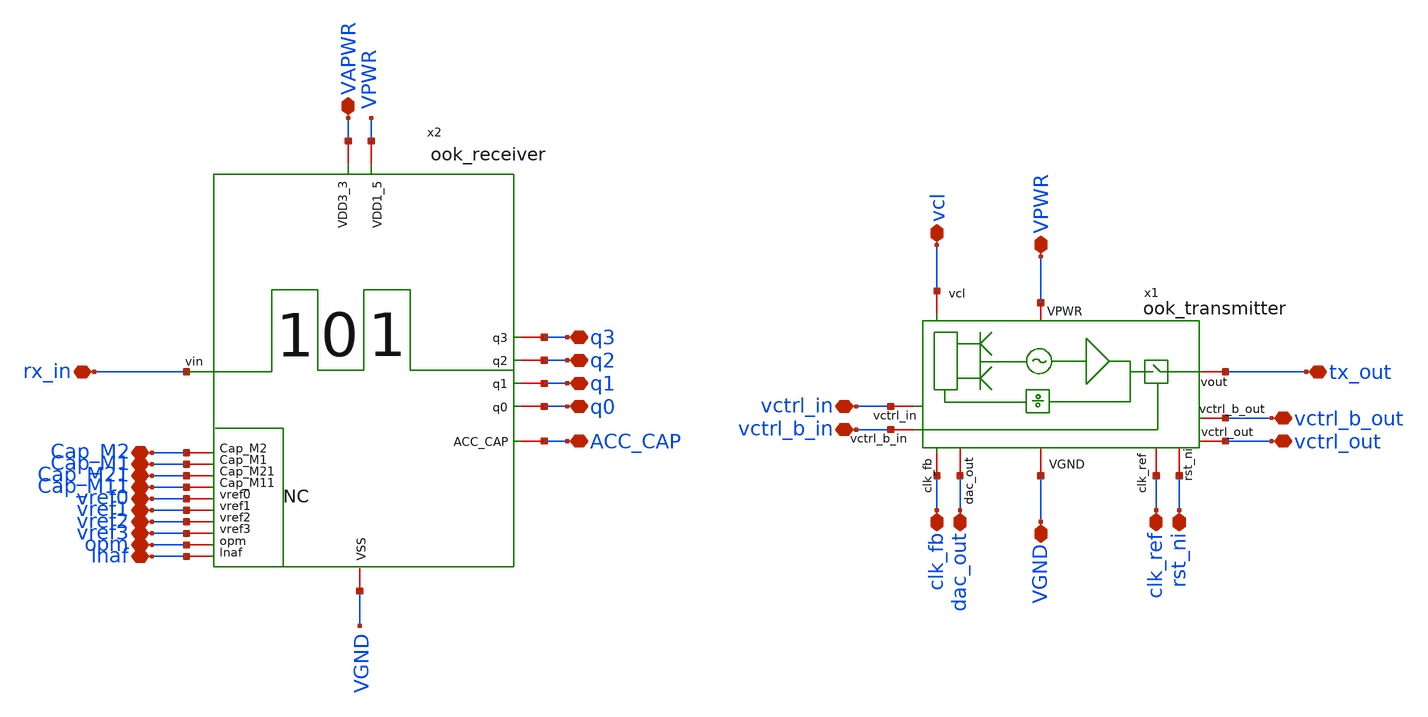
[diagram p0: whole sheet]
** sch_path: macros/heichips26_ook_top/macros/ook_analog_system/schematic/xschem/ook_analog_system.sch
**.subckt ook_analog_system tx_out VPWR VGND vcl dac_out clk_fb clk_ref rst_ni vctrl_in vctrl_b_in
*+ vctrl_out vctrl_b_out q0 q1 q2 q3 ACC_CAP rx_in VAPWR Cap_M2 Cap_M1 Cap_M21 Cap_M11 vref0 vref1 vref3 vref2
*+ opm lnaf
*.iopin tx_out
*.iopin VPWR
*.iopin VGND
*.iopin vcl
*.iopin dac_out
*.iopin clk_fb
*.iopin clk_ref
*.iopin rst_ni
*.iopin vctrl_in
*.iopin vctrl_b_in
*.iopin vctrl_out
*.iopin vctrl_b_out
*.iopin q0
*.iopin q1
*.iopin q2
*.iopin q3
*.iopin ACC_CAP
*.iopin rx_in
*.iopin VAPWR
*.iopin Cap_M2
*.iopin Cap_M1
*.iopin Cap_M21
*.iopin Cap_M11
*.iopin vref0
*.iopin vref1
*.iopin vref3
*.iopin vref2
*.iopin opm
*.iopin lnaf
x1 clk_ref rst_ni vctrl_in vctrl_b_in dac_out clk_fb vcl VGND VPWR tx_out vctrl_out vctrl_b_out
+ ook_transmitter
x2 VPWR opm q0 vref0 q1 vref1 ACC_CAP q2 vref2 vref3 q3 VAPWR Cap_M11 Cap_M21 Cap_M1 Cap_M2 rx_in
+ VGND lnaf ook_receiver
**.ends
.end
